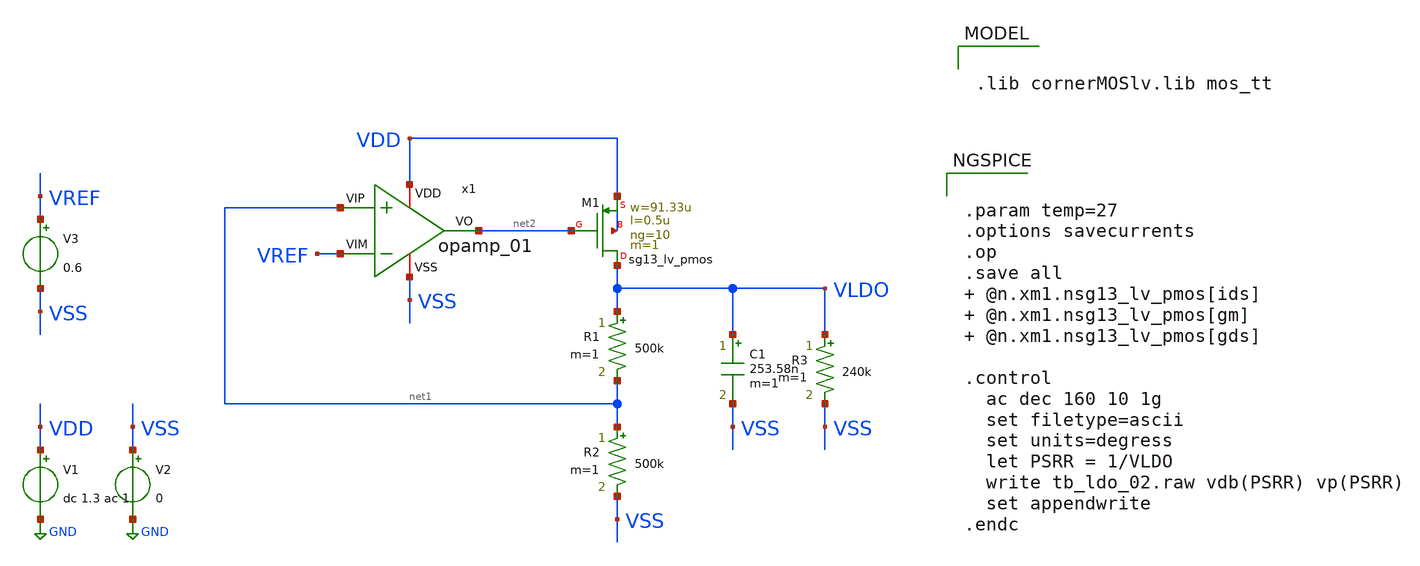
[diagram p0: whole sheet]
** sch_path: analog/tb/tb_ldo_01.sch
**.subckt tb_ldo_01
C1 VLDO VSS 253.58n m=1
V1 VDD GND dc 1.3 ac 1
V2 VSS GND 0
V3 VREF VSS 0.6
x1 VDD net1 net2 VSS VREF opamp_01
XM1 VLDO net2 VDD VDD sg13_lv_pmos w=91.33u l=0.5u ng=10 m=1 mm_ok=1
R2 net1 VSS 500k m=1
R1 VLDO net1 500k m=1
R3 VLDO VSS 240k m=1
**** begin user architecture code


.param temp=27
.options savecurrents
.op
.save all  @n.xm1.nsg13_lv_pmos[ids]  @n.xm1.nsg13_lv_pmos[gm]  @n.xm1.nsg13_lv_pmos[gds]

.control
  ac dec 160 10 1g
  set filetype=ascii
  set units=degress
  let PSRR = 1/VLDO
  write tb_ldo_02.raw vdb(PSRR) vp(PSRR)
  set appendwrite
.endc




.lib cornerMOSlv.lib mos_tt


**** end user architecture code
**.ends

* expanding   symbol:  opamp_01.sym # of pins=5
** sym_path: analog/core/opamp_01.sym
** sch_path: analog/core/opamp_01.sch
.subckt opamp_01 VDD VIP VO VSS VIM
*.iopin VIM
*.iopin VIP
*.iopin VSS
*.iopin VDD
*.iopin VO
XM1 net2 VIP net1 VSS sg13_lv_nmos w=10u l=0.25u ng=1 m=1 mm_ok=1
XM2 VO VIM net1 VSS sg13_lv_nmos w=10u l=0.25u ng=1 m=1 mm_ok=1
XM3 net2 net2 VDD VDD sg13_lv_pmos w=1u l=4u ng=1 m=1 mm_ok=1
XM4 VO net2 VDD VDD sg13_lv_pmos w=1u l=4u ng=1 m=1 mm_ok=1
XM5 net1 net3 VSS VSS sg13_lv_nmos w=2u l=2u ng=1 m=1 mm_ok=1
XM6 net3 net3 VSS VSS sg13_lv_nmos w=2u l=2u ng=1 m=1 mm_ok=1
I0 VDD net3 100n
.ends

.GLOBAL GND
.end
